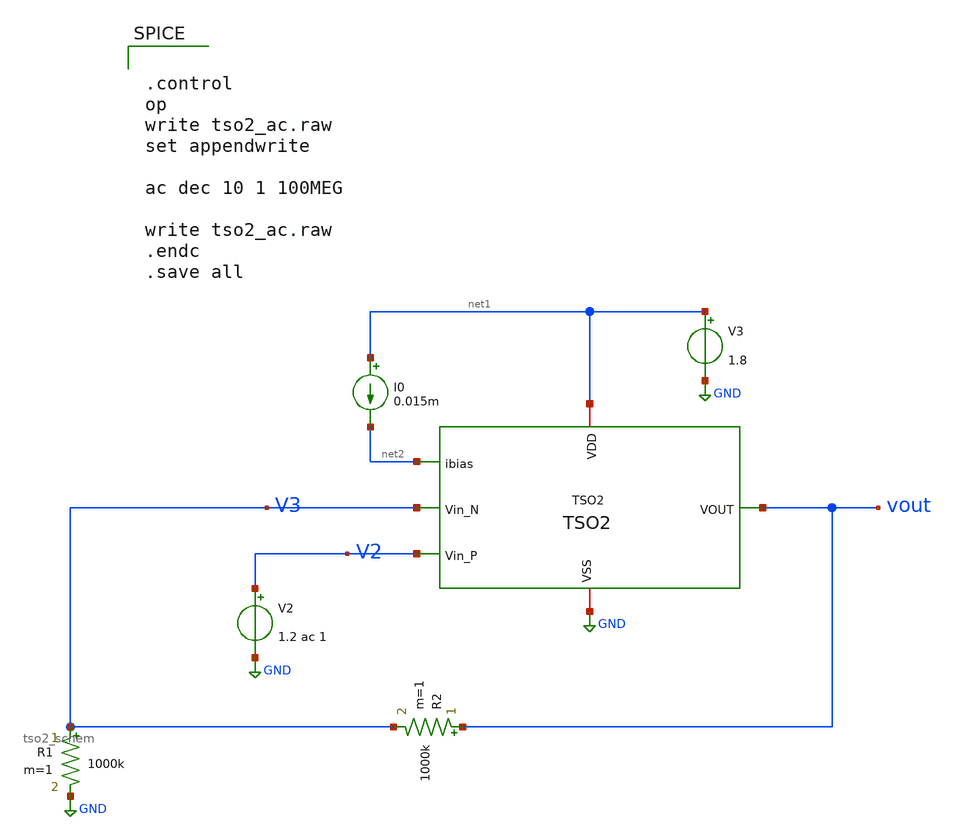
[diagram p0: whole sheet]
** sch_path: xschem/tso2_ac.sch
**.subckt tso2_ac
x1 vout V3 V2 net2 GND net1 tso2_schem
V2 V2 GND 1.2 ac 1
V3 net1 GND 1.8
I0 net1 net2 0.015m
R1 V3 GND 1000k m=1
R2 vout V3 1000k m=1
**** begin user architecture code

** opencircuitdesign pdks install
.lib $::SKYWATER_MODELS/sky130.lib.spice tt




.control
op
write tso2_ac.raw
set appendwrite

ac dec 10 1 100MEG

write tso2_ac.raw
.endc
.save all


**** end user architecture code
**.ends

* expanding   symbol:  tso2_schem.sym # of pins=6
** sym_path: xschem/tso2_schem.sym
** sch_path: xschem/tso2_schem.sch
.subckt tso2_schem VOUT Vin_N Vin_P ibias VSS VDD
*.opin VOUT
*.iopin VDD
*.iopin VSS
*.ipin ibias
*.ipin Vin_P
*.ipin Vin_N
XM1 net4 Vin_N vs1 GND sky130_fd_pr__nfet_01v8 L=0.5 W=1.5 nf=1 ad='int((nf+1)/2) * W/nf * 0.29' as='int((nf+2)/2) * W/nf * 0.29'
+ pd='2*int((nf+1)/2) * (W/nf + 0.29)' ps='2*int((nf+2)/2) * (W/nf + 0.29)' nrd='0.29 / W' nrs='0.29 / W'
+ sa=0 sb=0 sd=0 mult=1 m=1
XM2 net3 Vin_P vs1 GND sky130_fd_pr__nfet_01v8 L=0.5 W=1.5 nf=1 ad='int((nf+1)/2) * W/nf * 0.29' as='int((nf+2)/2) * W/nf * 0.29'
+ pd='2*int((nf+1)/2) * (W/nf + 0.29)' ps='2*int((nf+2)/2) * (W/nf + 0.29)' nrd='0.29 / W' nrs='0.29 / W'
+ sa=0 sb=0 sd=0 mult=1 m=1
XM3 vd1 vd1 VDD VDD sky130_fd_pr__pfet_01v8 L=0.5 W=1.5 nf=1 ad='int((nf+1)/2) * W/nf * 0.29' as='int((nf+2)/2) * W/nf * 0.29'
+ pd='2*int((nf+1)/2) * (W/nf + 0.29)' ps='2*int((nf+2)/2) * (W/nf + 0.29)' nrd='0.29 / W' nrs='0.29 / W'
+ sa=0 sb=0 sd=0 mult=1 m=1
XM4 vd2 vd1 VDD VDD sky130_fd_pr__pfet_01v8 L=0.5 W=1.5 nf=1 ad='int((nf+1)/2) * W/nf * 0.29' as='int((nf+2)/2) * W/nf * 0.29'
+ pd='2*int((nf+1)/2) * (W/nf + 0.29)' ps='2*int((nf+2)/2) * (W/nf + 0.29)' nrd='0.29 / W' nrs='0.29 / W'
+ sa=0 sb=0 sd=0 mult=1 m=1
XM5 net2 ibias VSS VSS sky130_fd_pr__nfet_01v8 L=0.5 W=4 nf=1 ad='int((nf+1)/2) * W/nf * 0.29' as='int((nf+2)/2) * W/nf * 0.29'
+ pd='2*int((nf+1)/2) * (W/nf + 0.29)' ps='2*int((nf+2)/2) * (W/nf + 0.29)' nrd='0.29 / W' nrs='0.29 / W'
+ sa=0 sb=0 sd=0 mult=1 m=1
XM6 net1 vg6 VDD VDD sky130_fd_pr__pfet_01v8 L=0.5 W=30 nf=1 ad='int((nf+1)/2) * W/nf * 0.29' as='int((nf+2)/2) * W/nf * 0.29'
+ pd='2*int((nf+1)/2) * (W/nf + 0.29)' ps='2*int((nf+2)/2) * (W/nf + 0.29)' nrd='0.29 / W' nrs='0.29 / W'
+ sa=0 sb=0 sd=0 mult=1 m=1
XM7 VOUT ibias VSS VSS sky130_fd_pr__nfet_01v8 L=1.75 W=36 nf=1 ad='int((nf+1)/2) * W/nf * 0.29' as='int((nf+2)/2) * W/nf * 0.29'
+ pd='2*int((nf+1)/2) * (W/nf + 0.29)' ps='2*int((nf+2)/2) * (W/nf + 0.29)' nrd='0.29 / W' nrs='0.29 / W'
+ sa=0 sb=0 sd=0 mult=1 m=1
XM8 ibias ibias VSS VSS sky130_fd_pr__nfet_01v8 L=0.5 W=4 nf=1 ad='int((nf+1)/2) * W/nf * 0.29' as='int((nf+2)/2) * W/nf * 0.29'
+ pd='2*int((nf+1)/2) * (W/nf + 0.29)' ps='2*int((nf+2)/2) * (W/nf + 0.29)' nrd='0.29 / W' nrs='0.29 / W'
+ sa=0 sb=0 sd=0 mult=1 m=1
XC1 vg6 net1 sky130_fd_pr__cap_mim_m3_1 W=19.4 L=19.4 MF=4 m=4
XC2 VOUT VSS sky130_fd_pr__cap_mim_m3_1 W=25 L=25 MF=8 m=8
v5 vd1 net4 0
.save i(v5)
v1 vs1 net2 0
.save i(v1)
v2 vd2 net3 0
.save i(v2)
v3 vd2 vg6 0
.save i(v3)
v4 net1 VOUT 0
.save i(v4)
.ends

.GLOBAL GND
.end
